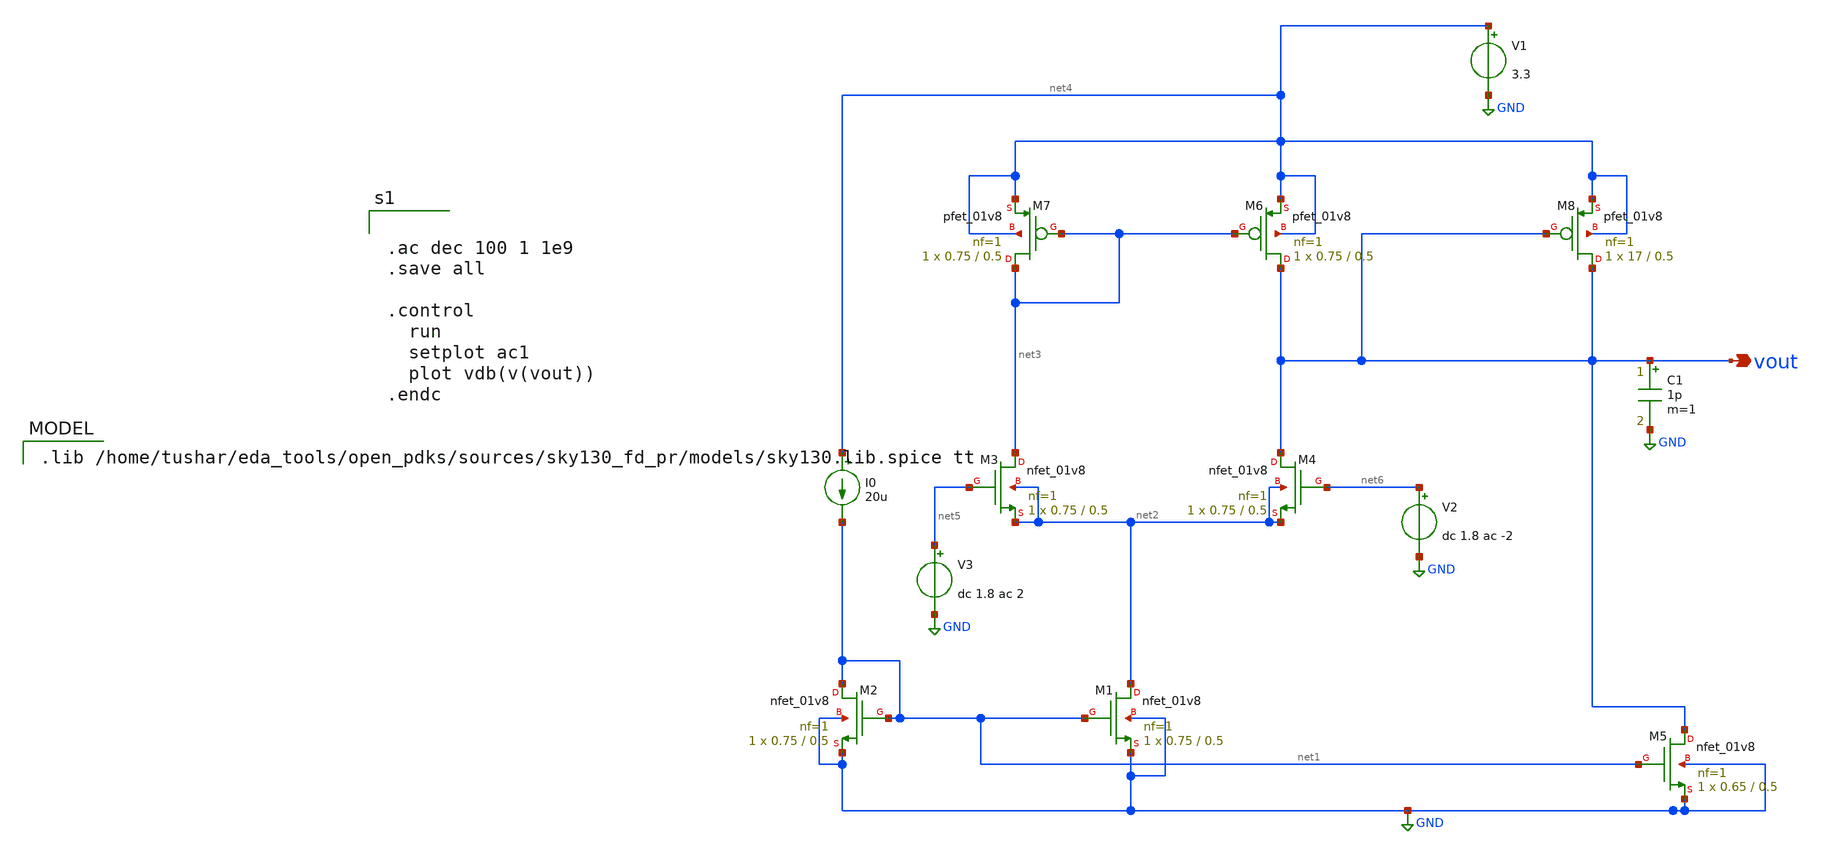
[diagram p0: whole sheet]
** sch_path: 11t_opamp/two_stage_improved.sch
**.subckt two_stage_improved vout
*.opin vout
XM1 net2 net1 GND GND sky130_fd_pr__nfet_01v8 L=0.5 W=0.75 nf=1 ad='int((1 + 1)/2) * 0.75 / 1 * 0.29'
+ as='int((1 + 2)/2) * 0.75 / 1 * 0.29' pd='2*int((1 + 1)/2) * (0.75 / 1 + 0.29)' ps='2*int((1 + 2)/2) * (0.75 / 1 + 0.29)'
+ nrd='0.29 / 0.75 ' nrs='0.29 / 0.75 ' sa=0 sb=0 sd=0 mult=1 m=1
XM2 net1 net1 GND GND sky130_fd_pr__nfet_01v8 L=0.5 W=0.75 nf=1 ad='int((1 + 1)/2) * 0.75 / 1 * 0.29'
+ as='int((1 + 2)/2) * 0.75 / 1 * 0.29' pd='2*int((1 + 1)/2) * (0.75 / 1 + 0.29)' ps='2*int((1 + 2)/2) * (0.75 / 1 + 0.29)'
+ nrd='0.29 / 0.75 ' nrs='0.29 / 0.75 ' sa=0 sb=0 sd=0 mult=1 m=1
XM3 net3 net5 net2 net2 sky130_fd_pr__nfet_01v8 L=0.5 W=0.75 nf=1 ad='int((1 + 1)/2) * 0.75 / 1 * 0.29'
+ as='int((1 + 2)/2) * 0.75 / 1 * 0.29' pd='2*int((1 + 1)/2) * (0.75 / 1 + 0.29)' ps='2*int((1 + 2)/2) * (0.75 / 1 + 0.29)'
+ nrd='0.29 / 0.75 ' nrs='0.29 / 0.75 ' sa=0 sb=0 sd=0 mult=1 m=1
XM4 vout net6 net2 net2 sky130_fd_pr__nfet_01v8 L=0.5 W=0.75 nf=1 ad='int((1 + 1)/2) * 0.75 / 1 * 0.29'
+ as='int((1 + 2)/2) * 0.75 / 1 * 0.29' pd='2*int((1 + 1)/2) * (0.75 / 1 + 0.29)' ps='2*int((1 + 2)/2) * (0.75 / 1 + 0.29)'
+ nrd='0.29 / 0.75 ' nrs='0.29 / 0.75 ' sa=0 sb=0 sd=0 mult=1 m=1
XM5 vout net1 GND GND sky130_fd_pr__nfet_01v8 L=0.5 W=0.65 nf=1 ad='int((1 + 1)/2) * 0.65 / 1 * 0.29'
+ as='int((1 + 2)/2) * 0.65 / 1 * 0.29' pd='2*int((1 + 1)/2) * (0.65 / 1 + 0.29)' ps='2*int((1 + 2)/2) * (0.65 / 1 + 0.29)'
+ nrd='0.29 / 0.65 ' nrs='0.29 / 0.65 ' sa=0 sb=0 sd=0 mult=1 m=1
XM6 vout net3 net4 net4 sky130_fd_pr__pfet_01v8 L=0.5 W=0.75 nf=1 ad='int((1 + 1)/2) * 0.75 / 1 * 0.29'
+ as='int((1 + 2)/2) * 0.75 / 1 * 0.29' pd='2*int((1 + 1)/2) * (0.75 / 1 + 0.29)' ps='2*int((1 + 2)/2) * (0.75 / 1 + 0.29)'
+ nrd='0.29 / 0.75 ' nrs='0.29 / 0.75 ' sa=0 sb=0 sd=0 mult=1 m=1
XM7 net3 net3 net4 net4 sky130_fd_pr__pfet_01v8 L=0.5 W=0.75 nf=1 ad='int((1 + 1)/2) * 0.75 / 1 * 0.29'
+ as='int((1 + 2)/2) * 0.75 / 1 * 0.29' pd='2*int((1 + 1)/2) * (0.75 / 1 + 0.29)' ps='2*int((1 + 2)/2) * (0.75 / 1 + 0.29)'
+ nrd='0.29 / 0.75 ' nrs='0.29 / 0.75 ' sa=0 sb=0 sd=0 mult=1 m=1
XM8 vout vout net4 net4 sky130_fd_pr__pfet_01v8 L=0.5 W=17 nf=1 ad='int((1 + 1)/2) * 17 / 1 * 0.29' as='int((1 + 2)/2) * 17 / 1 * 0.29'
+ pd='2*int((1 + 1)/2) * (17 / 1 + 0.29)' ps='2*int((1 + 2)/2) * (17 / 1 + 0.29)' nrd='0.29 / 17 ' nrs='0.29 / 17 '
+ sa=0 sb=0 sd=0 mult=1 m=1
C1 vout GND 1p m=1
V1 net4 GND 3.3
V2 net6 GND dc 1.8 ac -2
V3 net5 GND dc 1.8 ac 2
I0 net4 net1 20u
**** begin user architecture code


.ac dec 100 1 1e9
.save all

.control
  run
  setplot ac1
  plot vdb(v(vout))
.endc


.lib /home/tushar/eda_tools/open_pdks/sources/sky130_fd_pr/models/sky130.lib.spice tt

**** end user architecture code
**.ends
.GLOBAL GND
.end
